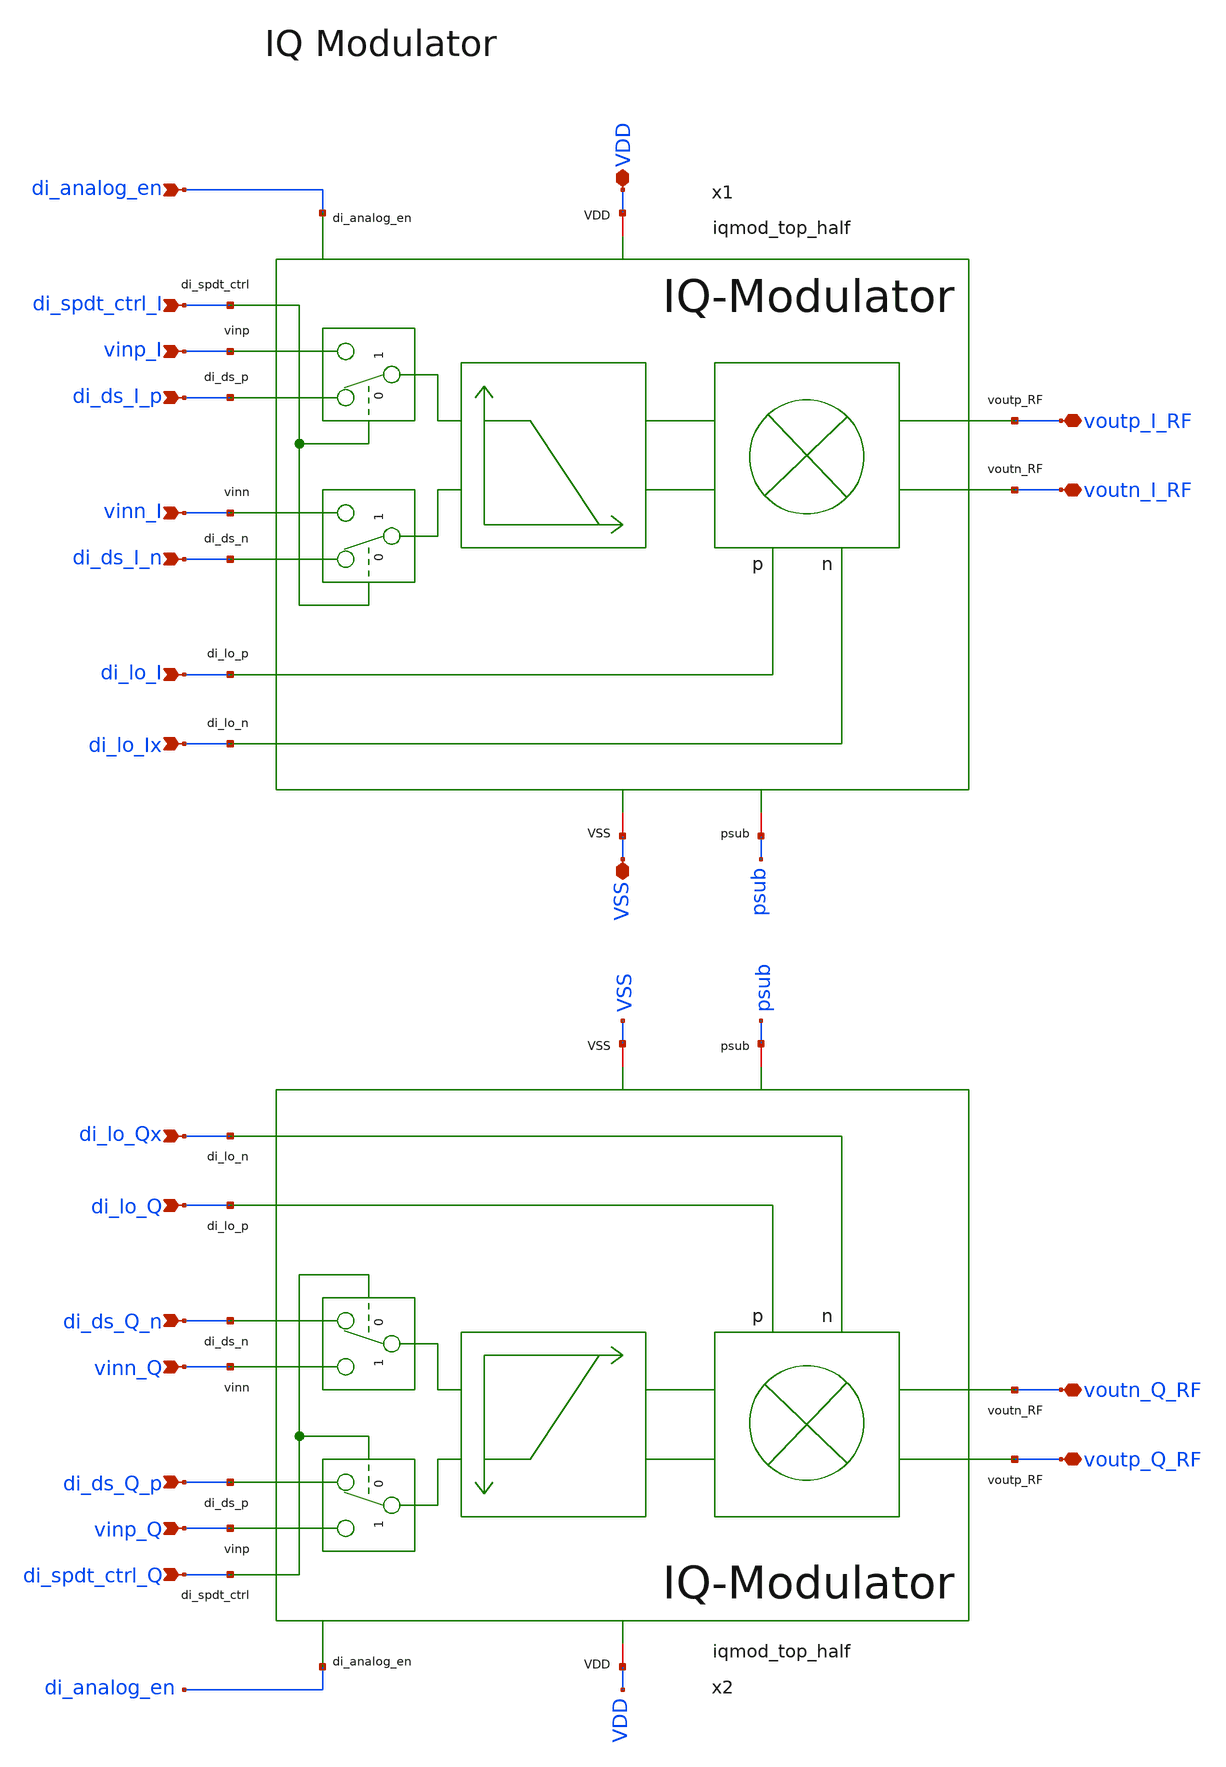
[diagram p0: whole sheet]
** sch_path: ihp130/macros/iqmod/schematic/iqmod_top.sch
**.subckt iqmod_top VDD voutp_I_RF VSS di_lo_Q di_lo_Qx di_lo_I di_lo_Ix di_ds_I_p voutn_I_RF
*+ voutp_Q_RF voutn_Q_RF di_analog_en vinp_I vinn_I di_spdt_ctrl_I di_ds_I_n di_ds_Q_p vinp_Q vinn_Q
*+ di_spdt_ctrl_Q di_ds_Q_n
*.iopin VDD
*.iopin voutp_I_RF
*.iopin VSS
*.ipin di_lo_Q
*.ipin di_lo_Qx
*.ipin di_lo_I
*.ipin di_lo_Ix
*.ipin di_ds_I_p
*.iopin voutn_I_RF
*.iopin voutp_Q_RF
*.iopin voutn_Q_RF
*.ipin di_analog_en
*.ipin vinp_I
*.ipin vinn_I
*.ipin di_spdt_ctrl_I
*.ipin di_ds_I_n
*.ipin di_ds_Q_p
*.ipin vinp_Q
*.ipin vinn_Q
*.ipin di_spdt_ctrl_Q
*.ipin di_ds_Q_n
x1 di_ds_I_p di_spdt_ctrl_I di_ds_I_n di_lo_I di_lo_Ix voutp_I_RF vinp_I vinn_I voutn_I_RF VDD VSS
+ di_analog_en psub iqmod_top_half
x2 di_ds_Q_p di_spdt_ctrl_Q di_ds_Q_n di_lo_Q di_lo_Qx voutp_Q_RF vinp_Q vinn_Q voutn_Q_RF VDD VSS
+ di_analog_en psub iqmod_top_half
**.ends
.end
